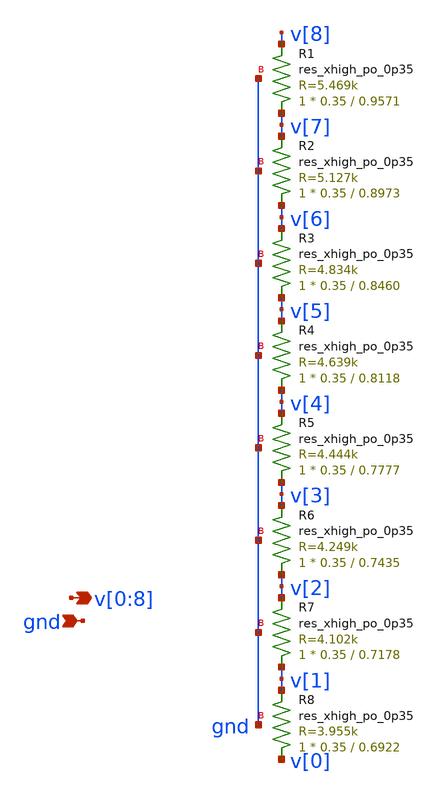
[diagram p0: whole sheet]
** sch_path: xschem/res_seg_3.sch
**.subckt res_seg_3 v[0],v[1],v[2],v[3],v[4],v[5],v[6],v[7],v[8] gnd
*.opin v[0],v[1],v[2],v[3],v[4],v[5],v[6],v[7],v[8]
*.ipin gnd
XR1 v[7] v[8] gnd sky130_fd_pr__res_xhigh_po_0p35 L=0.9571 mult=1 m=1
XR2 v[6] v[7] gnd sky130_fd_pr__res_xhigh_po_0p35 L=0.8973 mult=1 m=1
XR3 v[5] v[6] gnd sky130_fd_pr__res_xhigh_po_0p35 L=0.8460 mult=1 m=1
XR4 v[4] v[5] gnd sky130_fd_pr__res_xhigh_po_0p35 L=0.8118 mult=1 m=1
XR5 v[3] v[4] gnd sky130_fd_pr__res_xhigh_po_0p35 L=0.7777 mult=1 m=1
XR6 v[2] v[3] gnd sky130_fd_pr__res_xhigh_po_0p35 L=0.7435 mult=1 m=1
XR7 v[1] v[2] gnd sky130_fd_pr__res_xhigh_po_0p35 L=0.7178 mult=1 m=1
XR8 v[0] v[1] gnd sky130_fd_pr__res_xhigh_po_0p35 L=0.6922 mult=1 m=1
**.ends
.end
